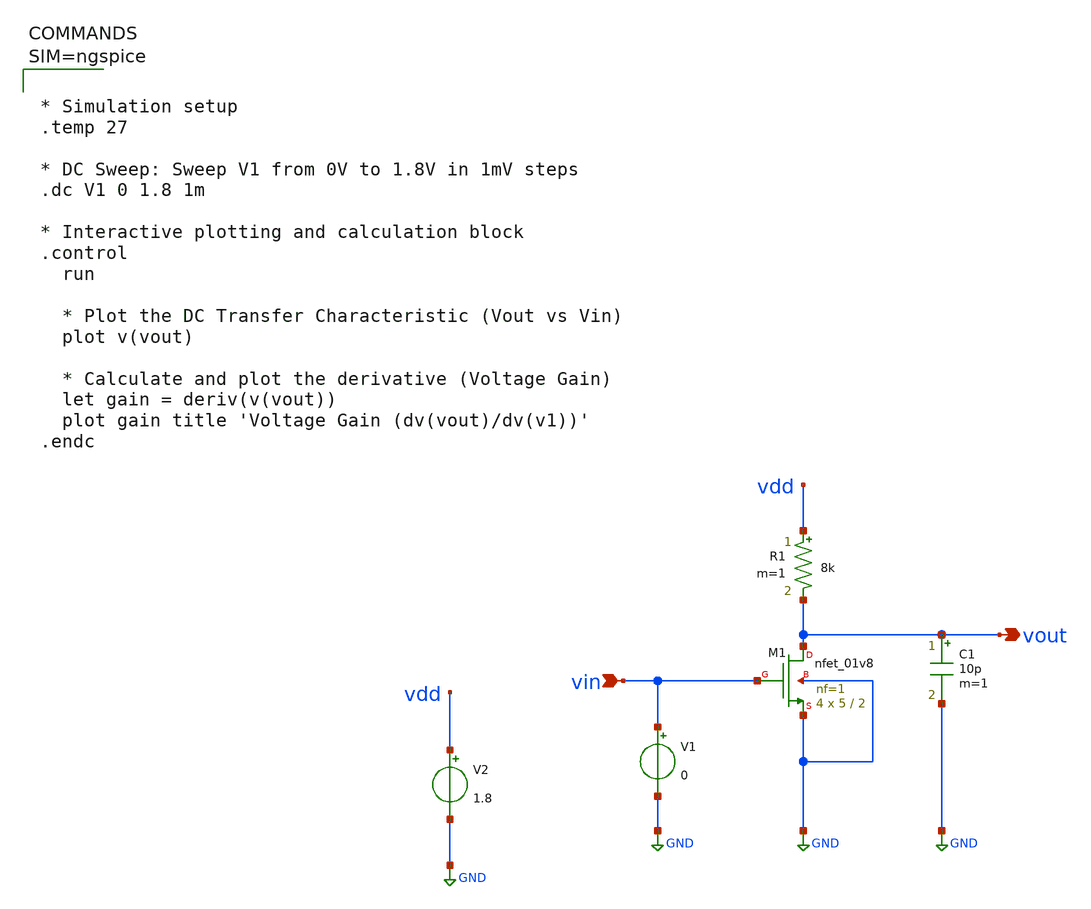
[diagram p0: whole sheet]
** sch_path: sch/NMOS_Restitive_Load_DC_Sweep.sch
**.subckt NMOS_Restitive_Load_DC_Sweep vout vin
*.opin vout
*.ipin vin
XM1 vout vin GND GND sky130_fd_pr__nfet_01v8 L=2 W=5 nf=1 ad='int((1 + 1)/2) * 5 / 1 * 0.29' as='int((1 + 2)/2) * 5 / 1 * 0.29'
+ pd='2*int((1 + 1)/2) * (5 / 1 + 0.29)' ps='2*int((1 + 2)/2) * (5 / 1 + 0.29)' nrd='0.29 / 5 ' nrs='0.29 / 5 '
+ sa=0 sb=0 sd=0 mult=4 m=4
R1 vdd vout 8k m=1
V1 vin GND 0
C1 vout GND 10p m=1
V2 vdd GND 1.8
**** begin user architecture code

** opencircuitdesign pdks install
.lib $::SKYWATER_MODELS/sky130.lib.spice tt




* Simulation setup
.temp 27

* DC Sweep: Sweep V1 from 0V to 1.8V in 1mV steps
.dc V1 0 1.8 1m

* Interactive plotting and calculation block
.control
  run

  * Plot the DC Transfer Characteristic (Vout vs Vin)
  plot v(vout)

  * Calculate and plot the derivative (Voltage Gain)
  let gain = deriv(v(vout))
  plot gain title 'Voltage Gain (dv(vout)/dv(v1))'
.endc



**** end user architecture code
**.ends
.GLOBAL GND
.end
